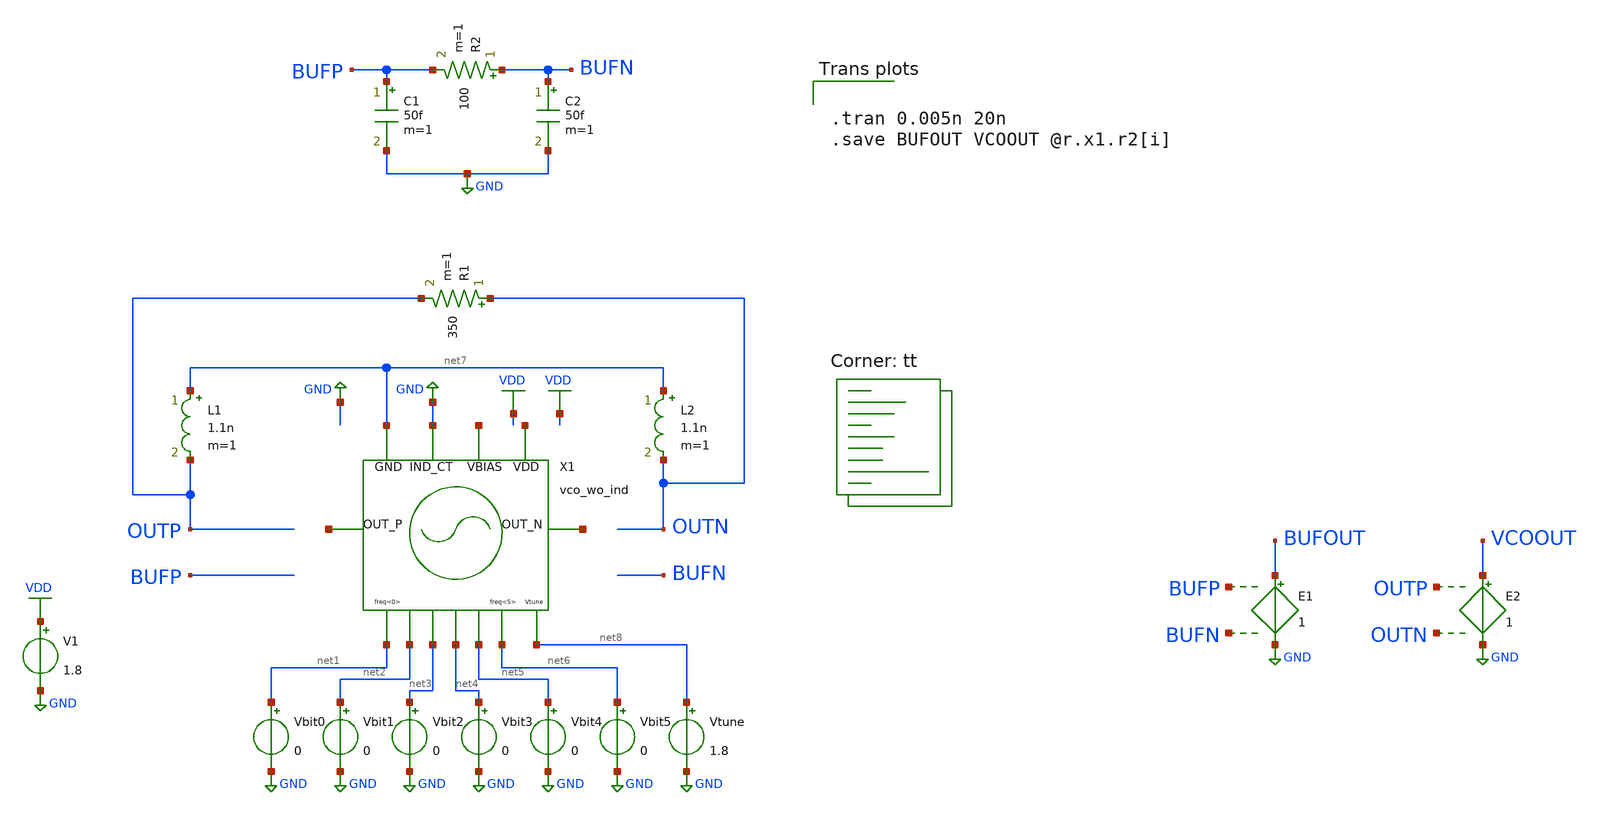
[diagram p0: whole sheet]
** sch_path: xschem/vco_wo_ind_tb.sch
* YI/C9Shc8z/CWPKLJb8BQD+O4ziO4wpAwbu7u7s7HEAy2IIt2IIlQD6O4ziO4ypAAICtDl/GPL8AgNZy7Go7vwAAAAAAAAAAAAAAAAAAAAAAAPeMn2NHvywNosQhFFq
**.subckt vco_wo_ind_tb
V1 VDD GND 1.8
Vbit0 net1 GND 0
Vbit1 net2 GND 0
Vbit2 net3 GND 0
Vbit3 net4 GND 0
Vbit4 net5 GND 0
Vbit5 net6 GND 0
L1 net7 OUTP 1.1n m=1
L2 net7 OUTN 1.1n m=1
Vtune net8 GND 1.8
R1 OUTN OUTP 350 m=1
R2 BUFN BUFP 100 m=1
C1 BUFP GND 50f m=1
C2 BUFN GND 50f m=1
E1 BUFOUT GND BUFP BUFN 1
E2 VCOOUT GND OUTP OUTN 1
X1 net9 net7 GND net10 net11 net1 net2 net3 net4 net5 net6 net12 net8 vco_wo_ind
**** begin user architecture code


.tran 0.005n 20n
.save BUFOUT VCOOUT @r.x1.r2[i]


.lib $::SKYWATER_MODELS/sky130.lib.spice tt
**** end user architecture code
**.ends
.GLOBAL GND
.GLOBAL VDD
.end
